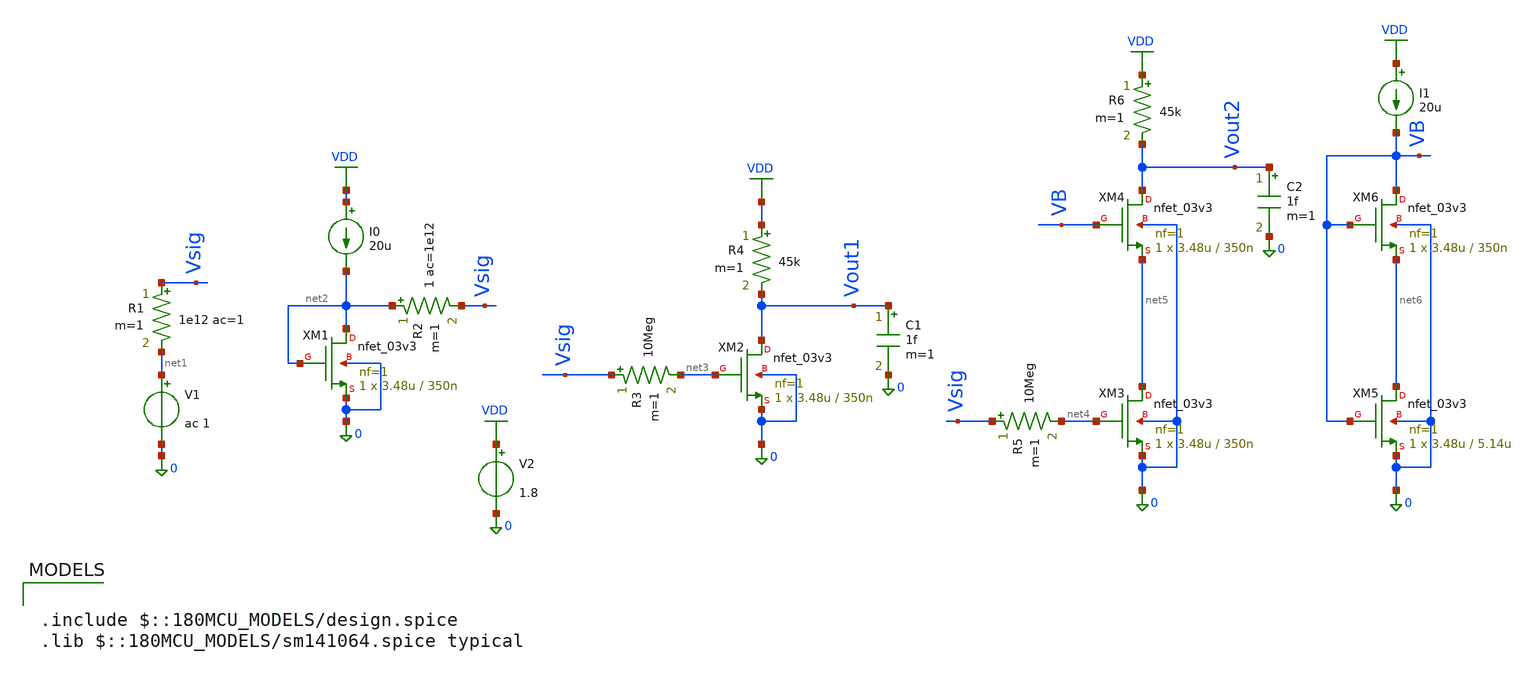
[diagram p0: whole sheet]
** sch_path: Lab_03/Cascode_forBW.sch
**.subckt Cascode_forBW
XM1 net2 net2 0 0 nfet_03v3 L=350n W=3.48u nf=1 ad='int((nf+1)/2) * W/nf * 0.18u' as='int((nf+2)/2) * W/nf * 0.18u'
+ pd='2*int((nf+1)/2) * (W/nf + 0.18u)' ps='2*int((nf+2)/2) * (W/nf + 0.18u)' nrd='0.18u / W' nrs='0.18u / W'
+ sa=0 sb=0 sd=0 m=1
V1 net1 0 ac 1
R1 Vsig net1 1e12 ac=1 m=1
C1 Vout1 0 1f m=1
V2 VDD 0 1.8
I0 VDD net2 20u
R2 net2 Vsig 1 ac=1e12 m=1
R3 Vsig net3 10Meg m=1
XM2 Vout1 net3 0 0 nfet_03v3 L=350n W=3.48u nf=1 ad='int((nf+1)/2) * W/nf * 0.18u' as='int((nf+2)/2) * W/nf * 0.18u'
+ pd='2*int((nf+1)/2) * (W/nf + 0.18u)' ps='2*int((nf+2)/2) * (W/nf + 0.18u)' nrd='0.18u / W' nrs='0.18u / W'
+ sa=0 sb=0 sd=0 m=1
R4 VDD Vout1 45k m=1
C2 Vout2 0 1f m=1
R5 Vsig net4 10Meg m=1
XM3 net5 net4 0 0 nfet_03v3 L=350n W=3.48u nf=1 ad='int((nf+1)/2) * W/nf * 0.18u' as='int((nf+2)/2) * W/nf * 0.18u'
+ pd='2*int((nf+1)/2) * (W/nf + 0.18u)' ps='2*int((nf+2)/2) * (W/nf + 0.18u)' nrd='0.18u / W' nrs='0.18u / W'
+ sa=0 sb=0 sd=0 m=1
R6 VDD Vout2 45k m=1
XM4 Vout2 VB net5 0 nfet_03v3 L=350n W=3.48u nf=1 ad='int((nf+1)/2) * W/nf * 0.18u' as='int((nf+2)/2) * W/nf * 0.18u'
+ pd='2*int((nf+1)/2) * (W/nf + 0.18u)' ps='2*int((nf+2)/2) * (W/nf + 0.18u)' nrd='0.18u / W' nrs='0.18u / W'
+ sa=0 sb=0 sd=0 m=1
XM5 net6 VB 0 0 nfet_03v3 L=5.14u W=3.48u nf=1 ad='int((nf+1)/2) * W/nf * 0.18u' as='int((nf+2)/2) * W/nf * 0.18u'
+ pd='2*int((nf+1)/2) * (W/nf + 0.18u)' ps='2*int((nf+2)/2) * (W/nf + 0.18u)' nrd='0.18u / W' nrs='0.18u / W'
+ sa=0 sb=0 sd=0 m=1
XM6 VB VB net6 0 nfet_03v3 L=350n W=3.48u nf=1 ad='int((nf+1)/2) * W/nf * 0.18u' as='int((nf+2)/2) * W/nf * 0.18u'
+ pd='2*int((nf+1)/2) * (W/nf + 0.18u)' ps='2*int((nf+2)/2) * (W/nf + 0.18u)' nrd='0.18u / W' nrs='0.18u / W'
+ sa=0 sb=0 sd=0 m=1
I1 VDD VB 20u
**** begin user architecture code

.include $::180MCU_MODELS/design.spice
.lib $::180MCU_MODELS/sm141064.spice typical


.control
alterparam sw_stat_global = 0
alterparam sw_stat_mismatch = 0
reset
save all

* Explicitly saving operating points to avoid loop expansion bugs
save @m.xm1.m0[id] @m.xm2.m0[id] @m.xm3.m0[id] @m.xm4.m0[id] @m.xm5.m0[id]
save @m.xm1.m0[vgs] @m.xm2.m0[vgs] @m.xm3.m0[vgs] @m.xm4.m0[vgs] @m.xm5.m0[vgs]
save @m.xm1.m0[vds] @m.xm2.m0[vds] @m.xm3.m0[vds] @m.xm4.m0[vds] @m.xm5.m0[vds]
save @m.xm1.m0[vdsat] @m.xm2.m0[vdsat] @m.xm3.m0[vdsat] @m.xm4.m0[vdsat] @m.xm5.m0[vdsat]
save @m.xm1.m0[vth] @m.xm2.m0[vth] @m.xm3.m0[vth] @m.xm4.m0[vth] @m.xm5.m0[vth]
save @m.xm1.m0[gm] @m.xm2.m0[gm] @m.xm3.m0[gm] @m.xm4.m0[gm] @m.xm5.m0[gm]
save @m.xm1.m0[gds] @m.xm2.m0[gds] @m.xm3.m0[gds] @m.xm4.m0[gds] @m.xm5.m0[gds]
save @m.xm1.m0[gmbs] @m.xm2.m0[gmbs] @m.xm3.m0[gmbs] @m.xm4.m0[gmbs] @m.xm5.m0[gmbs]
save @m.xm1.m0[cgg] @m.xm2.m0[cgg] @m.xm3.m0[cgg] @m.xm4.m0[cgg] @m.xm5.m0[cgg]
save @m.xm1.m0[cdd] @m.xm2.m0[cdd] @m.xm3.m0[cdd] @m.xm4.m0[cdd] @m.xm5.m0[cdd]
save @m.xm1.m0[css] @m.xm2.m0[css] @m.xm3.m0[css] @m.xm4.m0[css] @m.xm5.m0[css]
save @m.xm1.m0[cgs] @m.xm2.m0[cgs] @m.xm3.m0[cgs] @m.xm4.m0[cgs] @m.xm5.m0[cgs]
save @m.xm1.m0[cgd] @m.xm2.m0[cgd] @m.xm3.m0[cgd] @m.xm4.m0[cgd] @m.xm5.m0[cgd]

op
write lab_03_cascode_for_BW.raw

set appendwrite
ac dec 10 1 10G

meas ac DC_GAIN_1 find vmag(vout1) at=1
let A3db = DC_GAIN_1/sqrt(2)
meas ac BW_1 when vmag(vout1)=A3db fall=1
let GBW_1 = DC_GAIN_1 * BW_1
meas ac UGF_1 when vmag(vout1)=1 fall=1

meas ac DC_GAIN_2 find vmag(vout2) at=1
let A3db = DC_GAIN_2/sqrt(2)
meas ac BW_2 when vmag(vout2)=A3db fall=1
let GBW_2 = DC_GAIN_2 * BW_2
meas ac UGF_2 when vmag(vout2)=1 fall=1

print DC_GAIN_1 BW_1 GBW_1 UGF_1 > lab_03_results.txt
print DC_GAIN_2 BW_2 GBW_2 UGF_2 >> lab_03_results.txt

remzerovec
write lab_03_cascode_for_BW.raw
.endc

**** end user architecture code
**.ends
.GLOBAL VDD
.end
